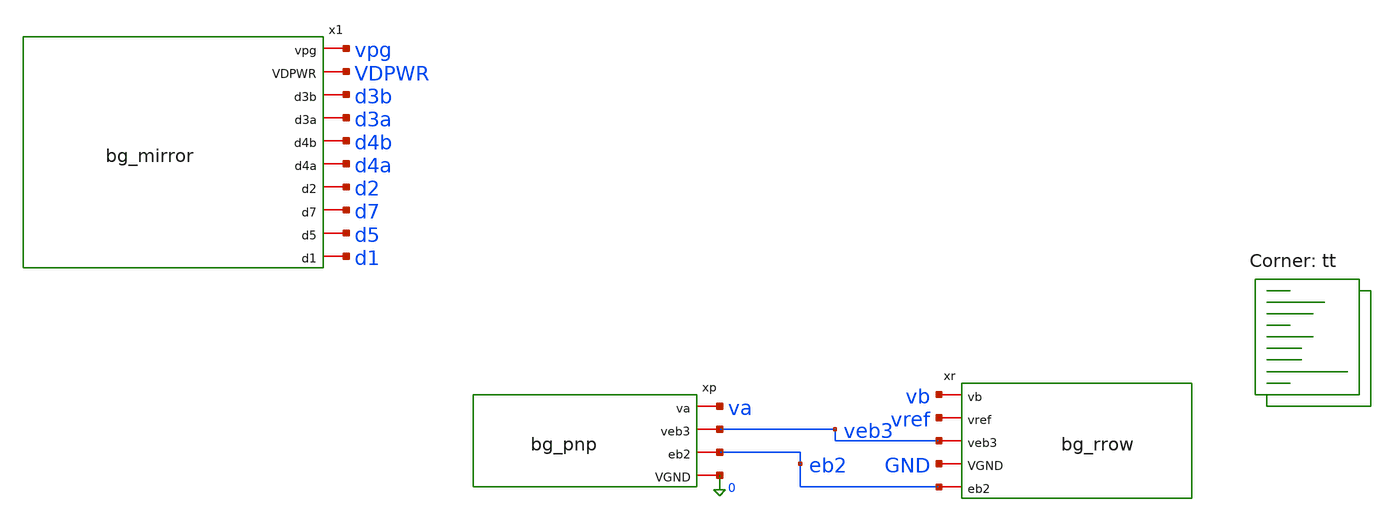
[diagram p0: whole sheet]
** sch_path: xschem/tb_bg_pol.sch
**.subckt tb_bg_pol
xp va veb3 eb2 0 bg_pnp
xr vb vref veb3 GND eb2 bg_rrow
x1 vpg VDPWR d3b d3a d4b d4a d2 d7 d5 d1 bg_mirror
**** begin user architecture code

Vdd VDPWR 0 1.8
* 0 V ammeters: each mirror drain -> the core node it feeds
Vm1 d1 va 0
Vm2 d2 vb 0
Vm3a d3a vref 0
Vm3b d3b vref 0
* the other copies get their real loads later; park their drains at 0.71 V
V4a d4a 0 0.71
V4b d4b 0 0.71
V7 d7 0 0.71
V5 d5 0 0.71
* stand-in op-amp: gain 1e6, GBW 100 kHz, output stops at the 1.8 V rail
* pol=1 puts + on vb (hand analysis, M5 0); 2c will use pol=-1 to swap the inputs
.param pol=1
Bgm 0 x I = pol*1e-4*(v(vb)-v(va))
Rx x 0 1e10
Cx x 0 159p
Bout oa 0 V = min(1.8, 0.9 + v(x))
Vkick vpg oa dc 0 ac 1 pwl(0 0 1u 0 1.001u 1m 2u 1m 2.001u 0)
.nodeset v(vpg)=0.55 v(va)=0.71 v(vb)=0.71 v(vref)=1.25 v(x)=-0.37
.control
* M5 2c: loop polarity. Same circuit, op-amp inputs normal (pol=1) then swapped (pol=-1)
option reltol=1e-6 vntol=1e-9 abstol=1e-15 method=gear
foreach p 1 -1
  alterparam pol=$p
  reset
  * reset puts temp back to 27, so set 25 after it
  option temp=25
  op
  let i1 = i(vm1)*1e6
  let xvpg = v(vpg)
  echo POL_OP pol=$p I1_uA=$&i1 vpg_V=$&xvpg
  * loop gain: Vkick breaks the loop between oa and vpg, so T = -v(oa)/v(vpg)
  ac dec 20 1m 10meg
  let T = -v(oa)/v(vpg)
  let Tmag = abs(T)
  let ph = 180/pi*cph(T)
  let ph0 = ph[0]
  let gdb0 = db(Tmag[0])
  meas ac fu when Tmag=1
  let fu_kHz = fu/1e3
  echo POL_AC pol=$p T_dB_at_1mHz=$&gdb0 phase_T_at_1mHz_deg=$&ph0 fu_kHz=$&fu_kHz
  * kick: +1 mV on vpg from 1 us to 2 us
  tran 10n 100u
  meas tran vpg_10 find v(vpg) at=10u
  meas tran vpg_end find v(vpg) at=100u
  meas tran i1_end find i(vm1) at=100u
  let i1e = i1_end*1e6
  echo POL_KICK pol=$p vpg_at_10us=$&vpg_10 vpg_at_100us=$&vpg_end I1_at_100us_uA=$&i1e
  plot v(vpg) title kick_pol_$p
end
.endc

.lib $::SKYWATER_MODELS/sky130.lib.spice tt
**** end user architecture code
**.ends

* expanding   symbol:  bg_pnp.sym # of pins=4
** sym_path: xschem/bg_pnp.sym
** sch_path: xschem/bg_pnp.sch
.subckt bg_pnp va veb3 eb2 VGND
*.iopin va
*.iopin eb2
*.iopin veb3
*.iopin VGND
XQ1 VGND VGND va sky130_fd_pr__pnp_05v5_W3p40L3p40 m=1
XQ2 VGND VGND eb2 sky130_fd_pr__pnp_05v5_W3p40L3p40 m=8
XQ3 VGND VGND veb3 sky130_fd_pr__pnp_05v5_W3p40L3p40 m=1
XQD VGND VGND VGND sky130_fd_pr__pnp_05v5_W3p40L3p40 m=15
.ends


* expanding   symbol:  bg_rrow.sym # of pins=5
** sym_path: xschem/bg_rrow.sym
** sch_path: xschem/bg_rrow.sch
.subckt bg_rrow vb vref veb3 VGND eb2
*.iopin vb
*.iopin eb2
*.iopin vref
*.iopin veb3
*.iopin VGND
XR1_1 eb2 net1 VGND sky130_fd_pr__res_high_po_1p41 L=20 mult=1 m=1
XR1_2 net1 net2 VGND sky130_fd_pr__res_high_po_1p41 L=20 mult=1 m=1
XR1_3 net2 net3 VGND sky130_fd_pr__res_high_po_1p41 L=20 mult=1 m=1
XR1_4 net3 vb VGND sky130_fd_pr__res_high_po_1p41 L=20 mult=1 m=1
XR3[39] r3n[38] vref VGND sky130_fd_pr__res_high_po_1p41 L=20 mult=1 m=1
XR3[38] r3n[37] r3n[38] VGND sky130_fd_pr__res_high_po_1p41 L=20 mult=1 m=1
XR3[37] r3n[36] r3n[37] VGND sky130_fd_pr__res_high_po_1p41 L=20 mult=1 m=1
XR3[36] r3n[35] r3n[36] VGND sky130_fd_pr__res_high_po_1p41 L=20 mult=1 m=1
XR3[35] r3n[34] r3n[35] VGND sky130_fd_pr__res_high_po_1p41 L=20 mult=1 m=1
XR3[34] r3n[33] r3n[34] VGND sky130_fd_pr__res_high_po_1p41 L=20 mult=1 m=1
XR3[33] r3n[32] r3n[33] VGND sky130_fd_pr__res_high_po_1p41 L=20 mult=1 m=1
XR3[32] r3n[31] r3n[32] VGND sky130_fd_pr__res_high_po_1p41 L=20 mult=1 m=1
XR3[31] r3n[30] r3n[31] VGND sky130_fd_pr__res_high_po_1p41 L=20 mult=1 m=1
XR3[30] r3n[29] r3n[30] VGND sky130_fd_pr__res_high_po_1p41 L=20 mult=1 m=1
XR3[29] r3n[28] r3n[29] VGND sky130_fd_pr__res_high_po_1p41 L=20 mult=1 m=1
XR3[28] r3n[27] r3n[28] VGND sky130_fd_pr__res_high_po_1p41 L=20 mult=1 m=1
XR3[27] r3n[26] r3n[27] VGND sky130_fd_pr__res_high_po_1p41 L=20 mult=1 m=1
XR3[26] r3n[25] r3n[26] VGND sky130_fd_pr__res_high_po_1p41 L=20 mult=1 m=1
XR3[25] r3n[24] r3n[25] VGND sky130_fd_pr__res_high_po_1p41 L=20 mult=1 m=1
XR3[24] r3n[23] r3n[24] VGND sky130_fd_pr__res_high_po_1p41 L=20 mult=1 m=1
XR3[23] r3n[22] r3n[23] VGND sky130_fd_pr__res_high_po_1p41 L=20 mult=1 m=1
XR3[22] r3n[21] r3n[22] VGND sky130_fd_pr__res_high_po_1p41 L=20 mult=1 m=1
XR3[21] r3n[20] r3n[21] VGND sky130_fd_pr__res_high_po_1p41 L=20 mult=1 m=1
XR3[20] r3n[19] r3n[20] VGND sky130_fd_pr__res_high_po_1p41 L=20 mult=1 m=1
XR3[19] r3n[18] r3n[19] VGND sky130_fd_pr__res_high_po_1p41 L=20 mult=1 m=1
XR3[18] r3n[17] r3n[18] VGND sky130_fd_pr__res_high_po_1p41 L=20 mult=1 m=1
XR3[17] r3n[16] r3n[17] VGND sky130_fd_pr__res_high_po_1p41 L=20 mult=1 m=1
XR3[16] r3n[15] r3n[16] VGND sky130_fd_pr__res_high_po_1p41 L=20 mult=1 m=1
XR3[15] r3n[14] r3n[15] VGND sky130_fd_pr__res_high_po_1p41 L=20 mult=1 m=1
XR3[14] r3n[13] r3n[14] VGND sky130_fd_pr__res_high_po_1p41 L=20 mult=1 m=1
XR3[13] r3n[12] r3n[13] VGND sky130_fd_pr__res_high_po_1p41 L=20 mult=1 m=1
XR3[12] r3n[11] r3n[12] VGND sky130_fd_pr__res_high_po_1p41 L=20 mult=1 m=1
XR3[11] r3n[10] r3n[11] VGND sky130_fd_pr__res_high_po_1p41 L=20 mult=1 m=1
XR3[10] r3n[9] r3n[10] VGND sky130_fd_pr__res_high_po_1p41 L=20 mult=1 m=1
XR3[9] r3n[8] r3n[9] VGND sky130_fd_pr__res_high_po_1p41 L=20 mult=1 m=1
XR3[8] r3n[7] r3n[8] VGND sky130_fd_pr__res_high_po_1p41 L=20 mult=1 m=1
XR3[7] r3n[6] r3n[7] VGND sky130_fd_pr__res_high_po_1p41 L=20 mult=1 m=1
XR3[6] r3n[5] r3n[6] VGND sky130_fd_pr__res_high_po_1p41 L=20 mult=1 m=1
XR3[5] r3n[4] r3n[5] VGND sky130_fd_pr__res_high_po_1p41 L=20 mult=1 m=1
XR3[4] r3n[3] r3n[4] VGND sky130_fd_pr__res_high_po_1p41 L=20 mult=1 m=1
XR3[3] r3n[2] r3n[3] VGND sky130_fd_pr__res_high_po_1p41 L=20 mult=1 m=1
XR3[2] r3n[1] r3n[2] VGND sky130_fd_pr__res_high_po_1p41 L=20 mult=1 m=1
XR3[1] r3n[0] r3n[1] VGND sky130_fd_pr__res_high_po_1p41 L=20 mult=1 m=1
XR3[0] veb3 r3n[0] VGND sky130_fd_pr__res_high_po_1p41 L=20 mult=1 m=1
XRD[3] VGND VGND VGND sky130_fd_pr__res_high_po_1p41 L=20 mult=1 m=1
XRD[2] VGND VGND VGND sky130_fd_pr__res_high_po_1p41 L=20 mult=1 m=1
XRD[1] VGND VGND VGND sky130_fd_pr__res_high_po_1p41 L=20 mult=1 m=1
XRD[0] VGND VGND VGND sky130_fd_pr__res_high_po_1p41 L=20 mult=1 m=1
.ends


* expanding   symbol:  bg_mirror.sym # of pins=10
** sym_path: xschem/bg_mirror.sym
** sch_path: xschem/bg_mirror.sch
.subckt bg_mirror vpg VDPWR d3b d3a d4b d4a d2 d7 d5 d1
*.iopin vpg
*.iopin VDPWR
*.iopin d1
*.iopin d2
*.iopin d3a
*.iopin d3b
*.iopin d4a
*.iopin d4b
*.iopin d7
*.iopin d5
XMP1 d1 vpg VDPWR VDPWR sky130_fd_pr__pfet_01v8 L=20 W=8.8 nf=1 ad='int((1 + 1)/2) * 8.8 / 1 * 0.29'
+ as='int((1 + 2)/2) * 8.8 / 1 * 0.29' pd='2*int((1 + 1)/2) * (8.8 / 1 + 0.29)' ps='2*int((1 + 2)/2) * (8.8 / 1 + 0.29)'
+ nrd='0.29 / 8.8 ' nrs='0.29 / 8.8 ' sa=0 sb=0 sd=0 mult=4 m=4
XMP2 d2 vpg VDPWR VDPWR sky130_fd_pr__pfet_01v8 L=20 W=8.8 nf=1 ad='int((1 + 1)/2) * 8.8 / 1 * 0.29'
+ as='int((1 + 2)/2) * 8.8 / 1 * 0.29' pd='2*int((1 + 1)/2) * (8.8 / 1 + 0.29)' ps='2*int((1 + 2)/2) * (8.8 / 1 + 0.29)'
+ nrd='0.29 / 8.8 ' nrs='0.29 / 8.8 ' sa=0 sb=0 sd=0 mult=4 m=4
XMP3A d3a vpg VDPWR VDPWR sky130_fd_pr__pfet_01v8 L=20 W=8.8 nf=1 ad='int((1 + 1)/2) * 8.8 / 1 * 0.29'
+ as='int((1 + 2)/2) * 8.8 / 1 * 0.29' pd='2*int((1 + 1)/2) * (8.8 / 1 + 0.29)' ps='2*int((1 + 2)/2) * (8.8 / 1 + 0.29)'
+ nrd='0.29 / 8.8 ' nrs='0.29 / 8.8 ' sa=0 sb=0 sd=0 mult=2 m=2
XMP3B d3b vpg VDPWR VDPWR sky130_fd_pr__pfet_01v8 L=20 W=8.8 nf=1 ad='int((1 + 1)/2) * 8.8 / 1 * 0.29'
+ as='int((1 + 2)/2) * 8.8 / 1 * 0.29' pd='2*int((1 + 1)/2) * (8.8 / 1 + 0.29)' ps='2*int((1 + 2)/2) * (8.8 / 1 + 0.29)'
+ nrd='0.29 / 8.8 ' nrs='0.29 / 8.8 ' sa=0 sb=0 sd=0 mult=2 m=2
XMP4A d4a vpg VDPWR VDPWR sky130_fd_pr__pfet_01v8 L=20 W=8.8 nf=1 ad='int((1 + 1)/2) * 8.8 / 1 * 0.29'
+ as='int((1 + 2)/2) * 8.8 / 1 * 0.29' pd='2*int((1 + 1)/2) * (8.8 / 1 + 0.29)' ps='2*int((1 + 2)/2) * (8.8 / 1 + 0.29)'
+ nrd='0.29 / 8.8 ' nrs='0.29 / 8.8 ' sa=0 sb=0 sd=0 mult=1 m=1
XMP4B d4b vpg VDPWR VDPWR sky130_fd_pr__pfet_01v8 L=20 W=8.8 nf=1 ad='int((1 + 1)/2) * 8.8 / 1 * 0.29'
+ as='int((1 + 2)/2) * 8.8 / 1 * 0.29' pd='2*int((1 + 1)/2) * (8.8 / 1 + 0.29)' ps='2*int((1 + 2)/2) * (8.8 / 1 + 0.29)'
+ nrd='0.29 / 8.8 ' nrs='0.29 / 8.8 ' sa=0 sb=0 sd=0 mult=1 m=1
XMP7 d7 vpg VDPWR VDPWR sky130_fd_pr__pfet_01v8 L=20 W=8.8 nf=1 ad='int((1 + 1)/2) * 8.8 / 1 * 0.29'
+ as='int((1 + 2)/2) * 8.8 / 1 * 0.29' pd='2*int((1 + 1)/2) * (8.8 / 1 + 0.29)' ps='2*int((1 + 2)/2) * (8.8 / 1 + 0.29)'
+ nrd='0.29 / 8.8 ' nrs='0.29 / 8.8 ' sa=0 sb=0 sd=0 mult=2 m=2
XMP5 d5 vpg VDPWR VDPWR sky130_fd_pr__pfet_01v8 L=20 W=8.8 nf=1 ad='int((1 + 1)/2) * 8.8 / 1 * 0.29'
+ as='int((1 + 2)/2) * 8.8 / 1 * 0.29' pd='2*int((1 + 1)/2) * (8.8 / 1 + 0.29)' ps='2*int((1 + 2)/2) * (8.8 / 1 + 0.29)'
+ nrd='0.29 / 8.8 ' nrs='0.29 / 8.8 ' sa=0 sb=0 sd=0 mult=2 m=2
.ends

.end
